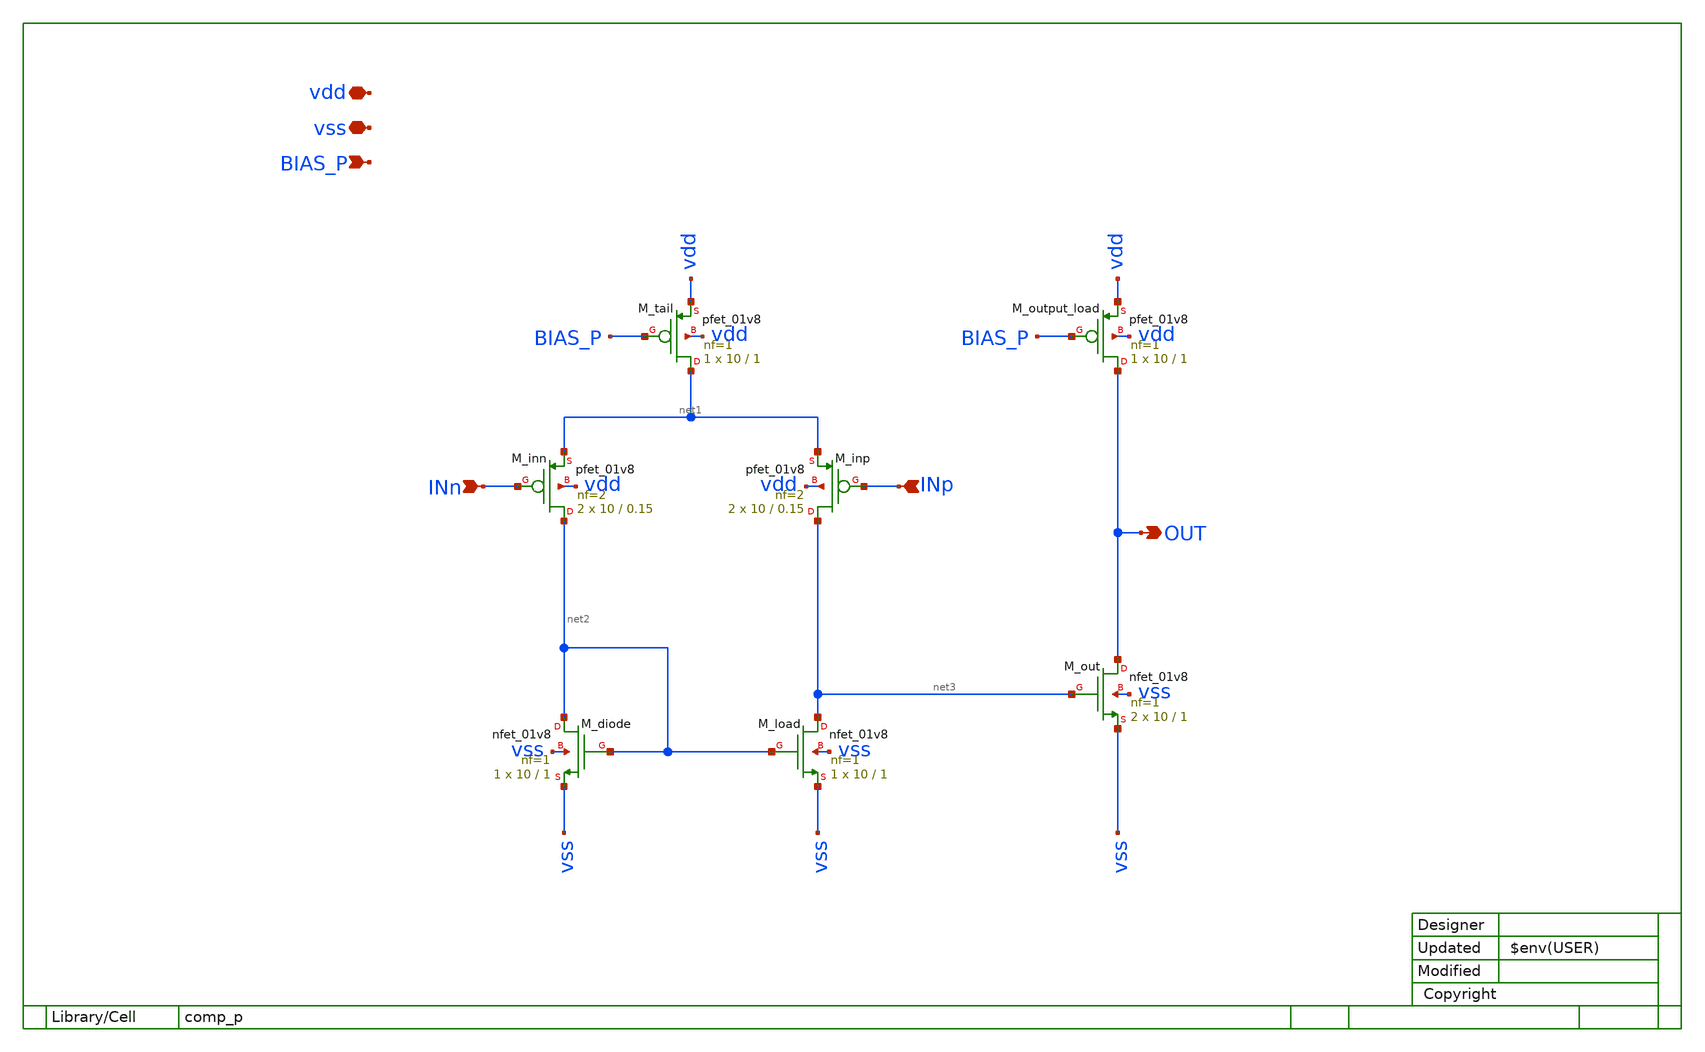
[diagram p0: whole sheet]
** sch_path: xsch/ip/comp_p.sch
**.subckt comp_p vdd OUT vss BIAS_P INn INp
*.iopin vdd
*.opin OUT
*.iopin vss
*.ipin BIAS_P
*.ipin INn
*.ipin INp
XM_load net3 net2 vss vss sky130_fd_pr__nfet_01v8 L=1 W=10 nf=1 ad='int((1 + 1)/2) * 10 / 1 * 0.29' as='int((1 + 2)/2) * 10 / 1 * 0.29'
+ pd='2*int((1 + 1)/2) * (10 / 1 + 0.29)' ps='2*int((1 + 2)/2) * (10 / 1 + 0.29)' nrd='0.29 / 10 ' nrs='0.29 / 10 '
+ sa=0 sb=0 sd=0 mult=1 m=1
XM_inn net2 INn net1 vdd sky130_fd_pr__pfet_01v8 L=0.15 W=10 nf=2 ad='int((nf+1)/2) * W/nf * 0.29' as='int((nf+2)/2) * W/nf * 0.29'
+ pd='2*int((nf+1)/2) * (W/nf + 0.29)' ps='2*int((nf+2)/2) * (W/nf + 0.29)' nrd='0.29 / W' nrs='0.29 / W'
+ sa=0 sb=0 sd=0 mult=2 m=2
XM_inp net3 INp net1 vdd sky130_fd_pr__pfet_01v8 L=0.15 W=10 nf=2 ad='int((nf+1)/2) * W/nf * 0.29' as='int((nf+2)/2) * W/nf * 0.29'
+ pd='2*int((nf+1)/2) * (W/nf + 0.29)' ps='2*int((nf+2)/2) * (W/nf + 0.29)' nrd='0.29 / W' nrs='0.29 / W'
+ sa=0 sb=0 sd=0 mult=2 m=2
XM_tail net1 BIAS_P vdd vdd sky130_fd_pr__pfet_01v8 L=1 W=10 nf=1 ad='int((nf+1)/2) * W/nf * 0.29' as='int((nf+2)/2) * W/nf * 0.29'
+ pd='2*int((nf+1)/2) * (W/nf + 0.29)' ps='2*int((nf+2)/2) * (W/nf + 0.29)' nrd='0.29 / W' nrs='0.29 / W'
+ sa=0 sb=0 sd=0 mult=1 m=1
XM_diode net2 net2 vss vss sky130_fd_pr__nfet_01v8 L=1 W=10 nf=1 ad='int((1 + 1)/2) * 10 / 1 * 0.29'
+ as='int((1 + 2)/2) * 10 / 1 * 0.29' pd='2*int((1 + 1)/2) * (10 / 1 + 0.29)' ps='2*int((1 + 2)/2) * (10 / 1 + 0.29)'
+ nrd='0.29 / 10 ' nrs='0.29 / 10 ' sa=0 sb=0 sd=0 mult=1 m=1
XM_out OUT net3 vss vss sky130_fd_pr__nfet_01v8 L=1 W=10 nf=1 ad='int((1 + 1)/2) * 10 / 1 * 0.29' as='int((1 + 2)/2) * 10 / 1 * 0.29'
+ pd='2*int((1 + 1)/2) * (10 / 1 + 0.29)' ps='2*int((1 + 2)/2) * (10 / 1 + 0.29)' nrd='0.29 / 10 ' nrs='0.29 / 10 '
+ sa=0 sb=0 sd=0 mult=2 m=2
XM_output_load OUT BIAS_P vdd vdd sky130_fd_pr__pfet_01v8 L=1 W=10 nf=1 ad='int((nf+1)/2) * W/nf * 0.29'
+ as='int((nf+2)/2) * W/nf * 0.29' pd='2*int((nf+1)/2) * (W/nf + 0.29)' ps='2*int((nf+2)/2) * (W/nf + 0.29)'
+ nrd='0.29 / W' nrs='0.29 / W' sa=0 sb=0 sd=0 mult=1 m=1
**.ends
.end
